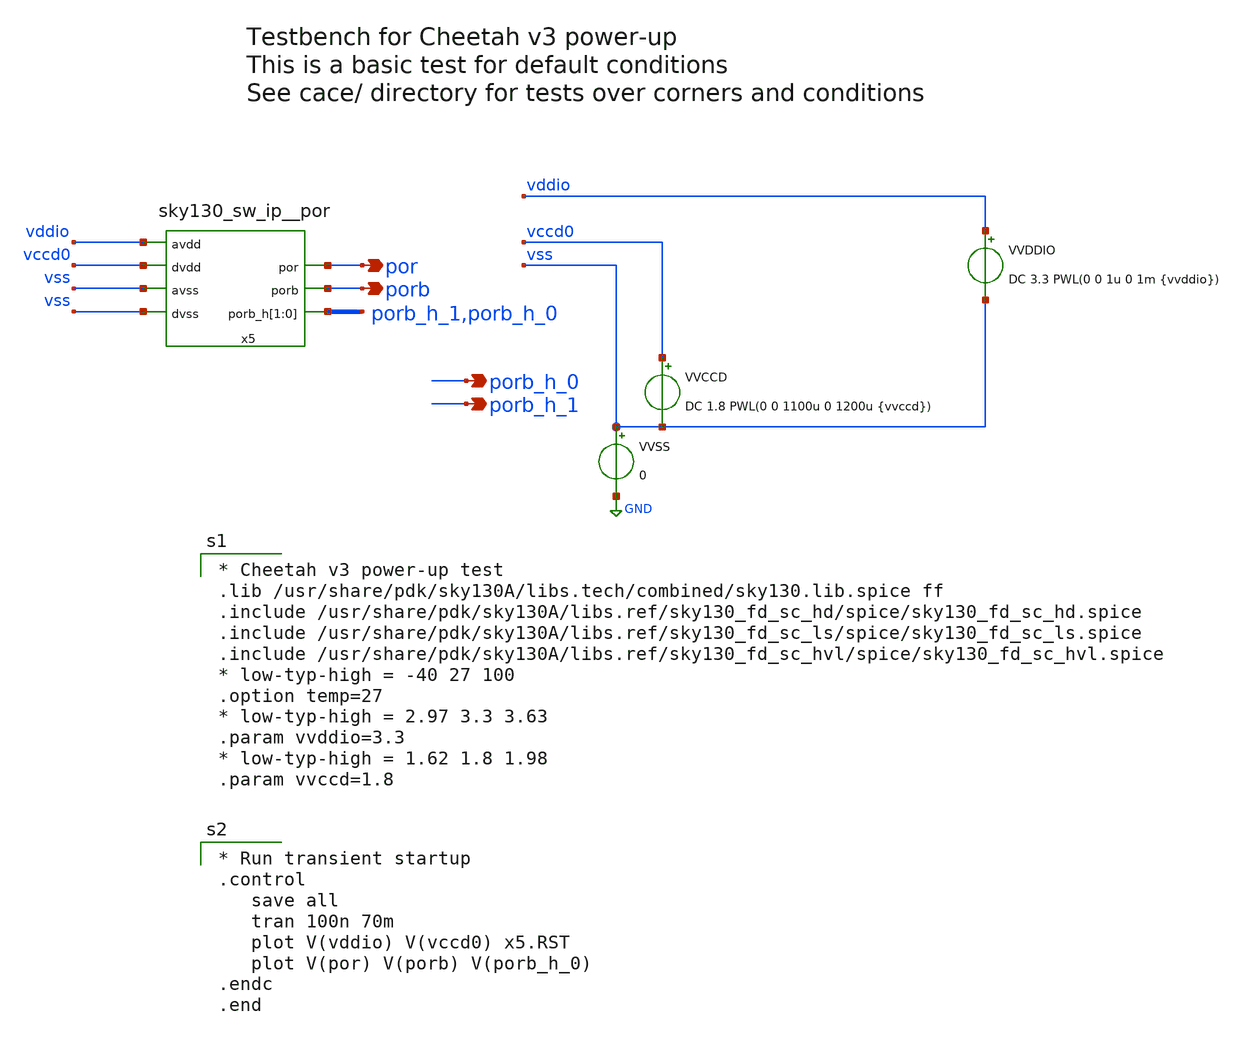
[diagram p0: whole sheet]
** sch_path: xschem/powerup_tb.sch
**.subckt powerup_tb por porb porb_h_0 porb_h_1
*.opin por
*.opin porb
*.opin porb_h_0
*.opin porb_h_1
VVDDIO vddio vss DC 3.3 PWL(0 0 1u 0 1m {vvddio})
VVCCD vccd0 vss DC 1.8 PWL(0 0 1100u 0 1200u {vvccd})
VVSS vss GND 0
x5 por vss vddio vccd0 porb vss porb_h_1 porb_h_0 sky130_sw_ip__por
**** begin user architecture code

* Cheetah v3 power-up test
.lib /usr/share/pdk/sky130A/libs.tech/combined/sky130.lib.spice ff
.include /usr/share/pdk/sky130A/libs.ref/sky130_fd_sc_hd/spice/sky130_fd_sc_hd.spice
.include /usr/share/pdk/sky130A/libs.ref/sky130_fd_sc_ls/spice/sky130_fd_sc_ls.spice
.include /usr/share/pdk/sky130A/libs.ref/sky130_fd_sc_hvl/spice/sky130_fd_sc_hvl.spice
* low-typ-high = -40 27 100
.option temp=27
* low-typ-high = 2.97 3.3 3.63
.param vvddio=3.3
* low-typ-high = 1.62 1.8 1.98
.param vvccd=1.8


* Run transient startup
.control
   save all
   tran 100n 70m
   plot V(vddio) V(vccd0) x5.RST
   plot V(por) V(porb) V(porb_h_0)
.endc
.end

**** end user architecture code
**.ends
.GLOBAL GND
.end
